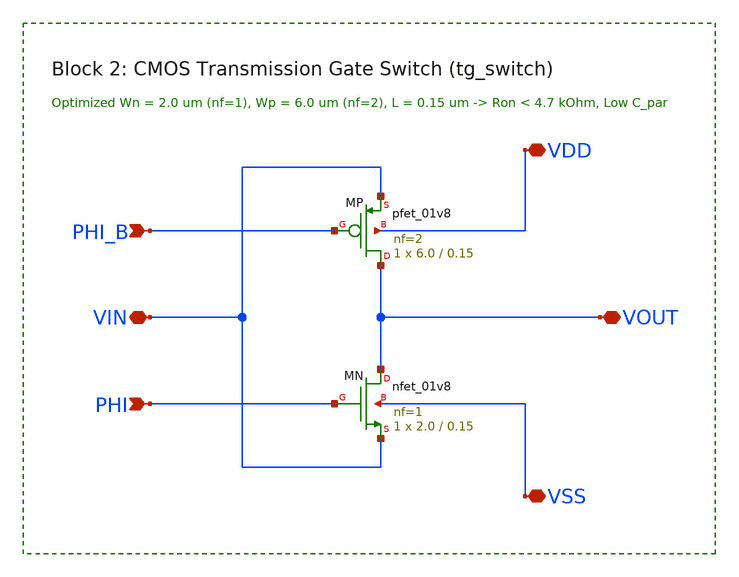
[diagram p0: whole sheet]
** sch_path: sky130-sc-lpf/xschem/tg_switch.sch
**.subckt tg_switch VIN VOUT PHI_B PHI VDD VSS
*.iopin VIN
*.iopin VOUT
*.ipin PHI_B
*.ipin PHI
*.iopin VDD
*.iopin VSS
XMP VOUT PHI_B VIN VDD sky130_fd_pr__pfet_01v8 L=0.15 W=6.0 nf=2 ad='int((nf+1)/2) * W/nf * 0.29' as='int((nf+2)/2) * W/nf * 0.29'
+ pd='2*int((nf+1)/2) * (W/nf + 0.29)' ps='2*int((nf+2)/2) * (W/nf + 0.29)' nrd='0.29 / W' nrs='0.29 / W'
+ sa=0 sb=0 sd=0 mult=1 m=1
XMN VOUT PHI VIN VSS sky130_fd_pr__nfet_01v8 L=0.15 W=2.0 nf=1 ad='int((1 + 1)/2) * 2.0 / 1 * 0.29' as='int((1 + 2)/2) * 2.0 / 1 * 0.29'
+ pd='2*int((1 + 1)/2) * (2.0 / 1 + 0.29)' ps='2*int((1 + 2)/2) * (2.0 / 1 + 0.29)' nrd='0.29 / 2.0 ' nrs='0.29 / 2.0 '
+ sa=0 sb=0 sd=0 mult=1 m=1
**.ends
.end
